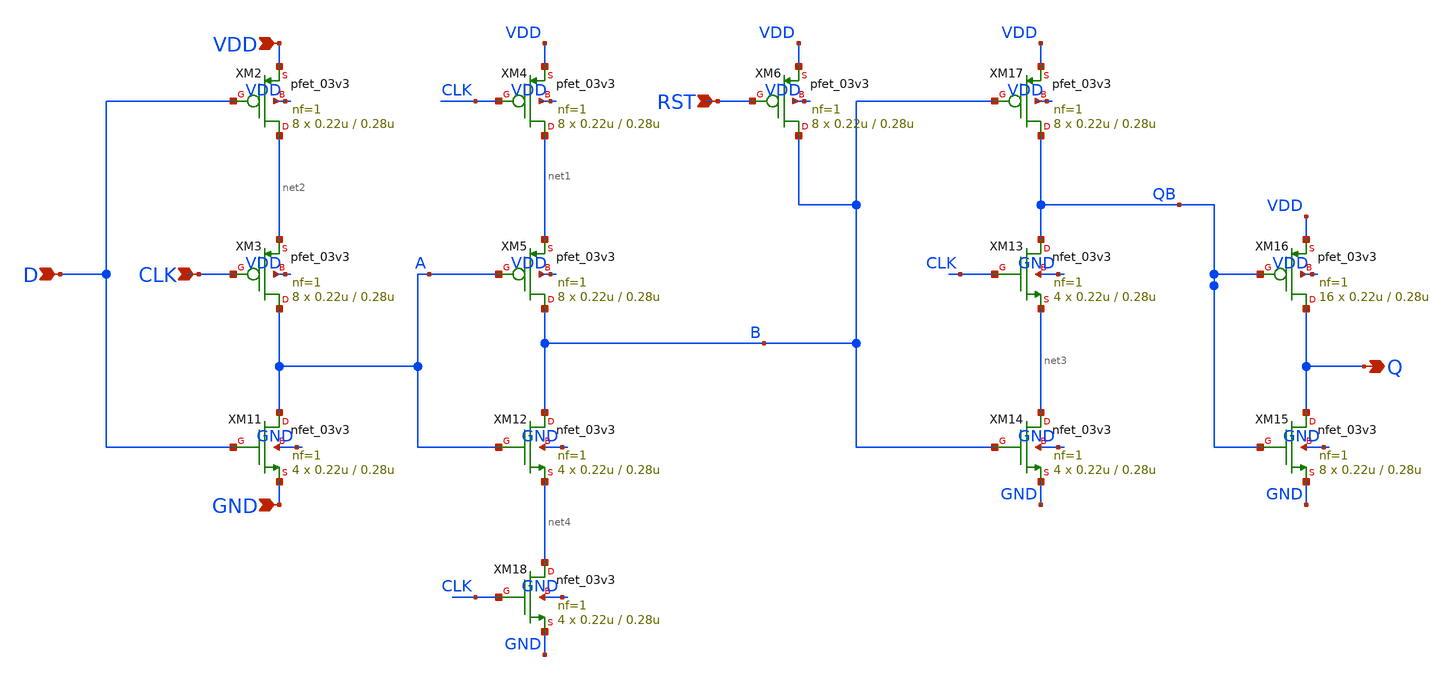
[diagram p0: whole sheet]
** sch_path: blocks/adc/encoder/sym/dff_encoder.sch
**.subckt dff_encoder Q D CLK RST VDD GND
*.opin Q
*.ipin D
*.ipin CLK
*.ipin RST
*.ipin VDD
*.ipin GND
XM2 net2 D VDD VDD pfet_03v3 L=0.28u W=0.22u nf=1 ad='int((nf+1)/2) * W/nf * 0.18u' as='int((nf+2)/2) * W/nf * 0.18u'
+ pd='2*int((nf+1)/2) * (W/nf + 0.18u)' ps='2*int((nf+2)/2) * (W/nf + 0.18u)' nrd='0.18u / W' nrs='0.18u / W'
+ sa=0 sb=0 sd=0 m=8
XM3 A CLK net2 VDD pfet_03v3 L=0.28u W=0.22u nf=1 ad='int((nf+1)/2) * W/nf * 0.18u' as='int((nf+2)/2) * W/nf * 0.18u'
+ pd='2*int((nf+1)/2) * (W/nf + 0.18u)' ps='2*int((nf+2)/2) * (W/nf + 0.18u)' nrd='0.18u / W' nrs='0.18u / W'
+ sa=0 sb=0 sd=0 m=8
XM4 net1 CLK VDD VDD pfet_03v3 L=0.28u W=0.22u nf=1 ad='int((nf+1)/2) * W/nf * 0.18u' as='int((nf+2)/2) * W/nf * 0.18u'
+ pd='2*int((nf+1)/2) * (W/nf + 0.18u)' ps='2*int((nf+2)/2) * (W/nf + 0.18u)' nrd='0.18u / W' nrs='0.18u / W'
+ sa=0 sb=0 sd=0 m=8
XM5 B A net1 VDD pfet_03v3 L=0.28u W=0.22u nf=1 ad='int((nf+1)/2) * W/nf * 0.18u' as='int((nf+2)/2) * W/nf * 0.18u'
+ pd='2*int((nf+1)/2) * (W/nf + 0.18u)' ps='2*int((nf+2)/2) * (W/nf + 0.18u)' nrd='0.18u / W' nrs='0.18u / W'
+ sa=0 sb=0 sd=0 m=8
XM6 B RST VDD VDD pfet_03v3 L=0.28u W=0.22u nf=1 ad='int((nf+1)/2) * W/nf * 0.18u' as='int((nf+2)/2) * W/nf * 0.18u'
+ pd='2*int((nf+1)/2) * (W/nf + 0.18u)' ps='2*int((nf+2)/2) * (W/nf + 0.18u)' nrd='0.18u / W' nrs='0.18u / W'
+ sa=0 sb=0 sd=0 m=8
XM11 A D GND GND nfet_03v3 L=0.28u W=0.22u nf=1 ad='int((nf+1)/2) * W/nf * 0.18u' as='int((nf+2)/2) * W/nf * 0.18u'
+ pd='2*int((nf+1)/2) * (W/nf + 0.18u)' ps='2*int((nf+2)/2) * (W/nf + 0.18u)' nrd='0.18u / W' nrs='0.18u / W'
+ sa=0 sb=0 sd=0 m=4
XM12 B A net4 GND nfet_03v3 L=0.28u W=0.22u nf=1 ad='int((nf+1)/2) * W/nf * 0.18u' as='int((nf+2)/2) * W/nf * 0.18u'
+ pd='2*int((nf+1)/2) * (W/nf + 0.18u)' ps='2*int((nf+2)/2) * (W/nf + 0.18u)' nrd='0.18u / W' nrs='0.18u / W'
+ sa=0 sb=0 sd=0 m=4
XM13 QB CLK net3 GND nfet_03v3 L=0.28u W=0.22u nf=1 ad='int((nf+1)/2) * W/nf * 0.18u' as='int((nf+2)/2) * W/nf * 0.18u'
+ pd='2*int((nf+1)/2) * (W/nf + 0.18u)' ps='2*int((nf+2)/2) * (W/nf + 0.18u)' nrd='0.18u / W' nrs='0.18u / W'
+ sa=0 sb=0 sd=0 m=4
XM14 net3 B GND GND nfet_03v3 L=0.28u W=0.22u nf=1 ad='int((nf+1)/2) * W/nf * 0.18u' as='int((nf+2)/2) * W/nf * 0.18u'
+ pd='2*int((nf+1)/2) * (W/nf + 0.18u)' ps='2*int((nf+2)/2) * (W/nf + 0.18u)' nrd='0.18u / W' nrs='0.18u / W'
+ sa=0 sb=0 sd=0 m=4
XM15 Q QB GND GND nfet_03v3 L=0.28u W=0.22u nf=1 ad='int((nf+1)/2) * W/nf * 0.18u' as='int((nf+2)/2) * W/nf * 0.18u'
+ pd='2*int((nf+1)/2) * (W/nf + 0.18u)' ps='2*int((nf+2)/2) * (W/nf + 0.18u)' nrd='0.18u / W' nrs='0.18u / W'
+ sa=0 sb=0 sd=0 m=8
XM16 Q QB VDD VDD pfet_03v3 L=0.28u W=0.22u nf=1 ad='int((nf+1)/2) * W/nf * 0.18u' as='int((nf+2)/2) * W/nf * 0.18u'
+ pd='2*int((nf+1)/2) * (W/nf + 0.18u)' ps='2*int((nf+2)/2) * (W/nf + 0.18u)' nrd='0.18u / W' nrs='0.18u / W'
+ sa=0 sb=0 sd=0 m=16
XM17 QB B VDD VDD pfet_03v3 L=0.28u W=0.22u nf=1 ad='int((nf+1)/2) * W/nf * 0.18u' as='int((nf+2)/2) * W/nf * 0.18u'
+ pd='2*int((nf+1)/2) * (W/nf + 0.18u)' ps='2*int((nf+2)/2) * (W/nf + 0.18u)' nrd='0.18u / W' nrs='0.18u / W'
+ sa=0 sb=0 sd=0 m=8
XM18 net4 CLK GND GND nfet_03v3 L=0.28u W=0.22u nf=1 ad='int((nf+1)/2) * W/nf * 0.18u' as='int((nf+2)/2) * W/nf * 0.18u'
+ pd='2*int((nf+1)/2) * (W/nf + 0.18u)' ps='2*int((nf+2)/2) * (W/nf + 0.18u)' nrd='0.18u / W' nrs='0.18u / W'
+ sa=0 sb=0 sd=0 m=4
**.ends
.end
